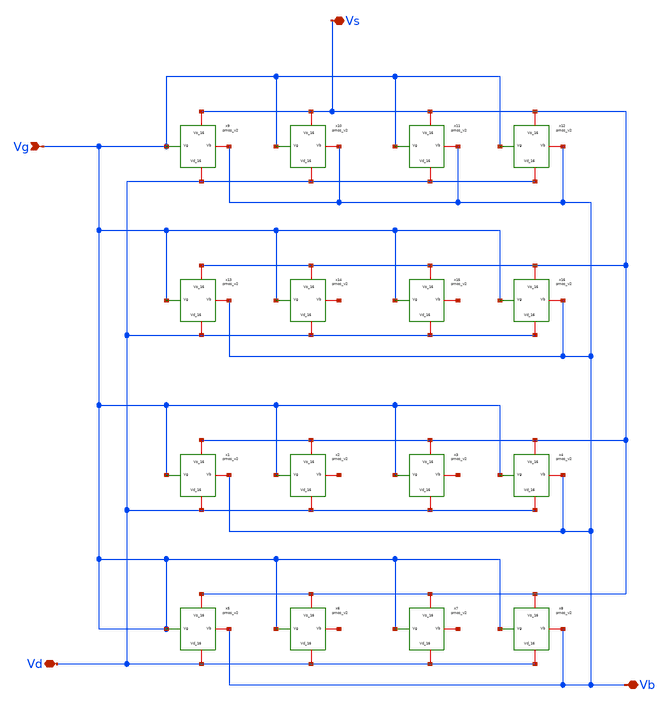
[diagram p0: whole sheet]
** sch_path: Layouts/PMOS/pmos_array_blocks.sch
**.subckt pmos_array_blocks Vg Vs Vd Vb
*.ipin Vg
*.iopin Vs
*.iopin Vd
*.iopin Vb
x1 Vs Vg Vb Vd pmos_v2
x2 Vs Vg net1 Vd pmos_v2
x3 Vs Vg net2 Vd pmos_v2
x4 Vs Vg Vb Vd pmos_v2
x5 Vs Vg Vb Vd pmos_v2
x6 Vs Vg net3 Vd pmos_v2
x7 Vs Vg net4 Vd pmos_v2
x8 Vs Vg Vb Vd pmos_v2
x9 Vs Vg Vb Vd pmos_v2
x10 Vs Vg Vb Vd pmos_v2
x11 Vs Vg Vb Vd pmos_v2
x12 Vs Vg Vb Vd pmos_v2
x13 Vs Vg Vb Vd pmos_v2
x14 Vs Vg net5 Vd pmos_v2
x15 Vs Vg net6 Vd pmos_v2
x16 Vs Vg Vb Vd pmos_v2
**.ends

* expanding   symbol:  /shared/designs/Layouts/PMOS/pmos_v2.sym # of pins=4
** sym_path: Layouts/PMOS/pmos_v2.sym
** sch_path: Layouts/PMOS/pmos_v2.sch
.subckt pmos_v2 Vs_16 Vg Vb Vd_16
*.ipin Vg
*.iopin Vs_16
*.iopin Vd_16
*.iopin Vb
XM1 Vd_16 Vg Vs_16 net1 sg13_lv_pmos w=86.4u l=0.13u ng=36 m=1 mm_ok=1
XR1 Vb net1 ntap1 R=5.213 w=62e-6 l=1e-6
XR2 Vb net1 ntap1 R=5.213 w=62e-6 l=1e-6
XR3 Vb net1 ntap1 R=5.213 w=62e-6 l=1e-6
.ends

.end
